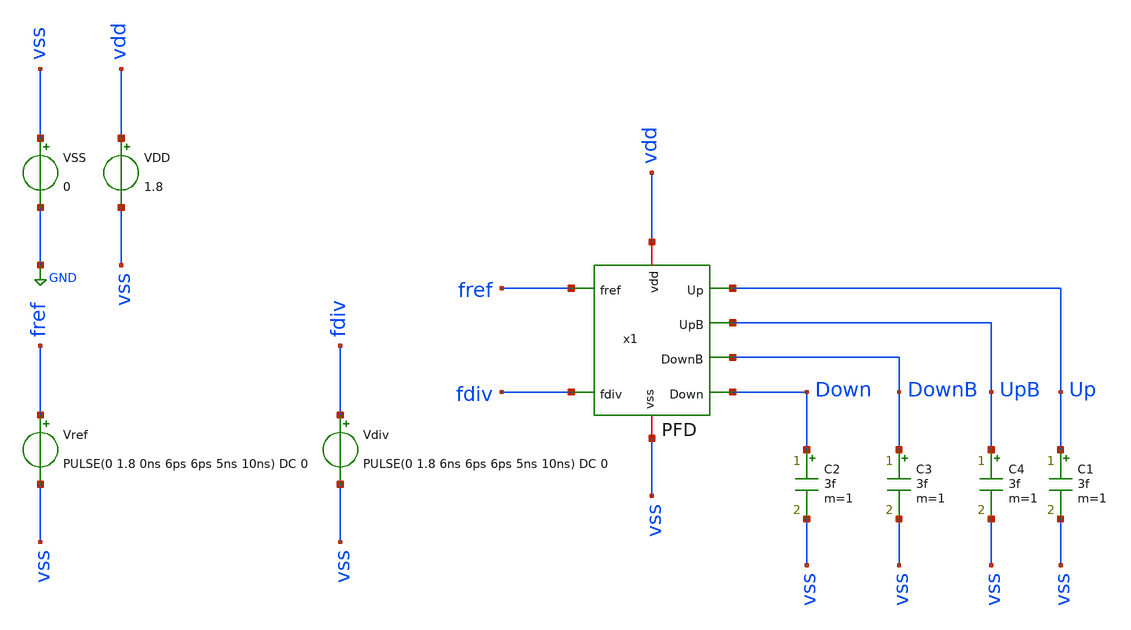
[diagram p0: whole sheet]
** sch_path: sch/PLL_caravel/tb_PFD.sch
**.subckt tb_PFD
VSS vss GND 0
VDD vdd vss 1.8
Vref fref vss PULSE(0 1.8 0ns 6ps 6ps 5ns 10ns) DC 0
Vdiv fdiv vss PULSE(0 1.8 6ns 6ps 6ps 5ns 10ns) DC 0
C1 Up vss 3f m=1
C2 Down vss 3f m=1
x1 vdd fref Up UpB DownB fdiv Down vss PFD
C3 DownB vss 3f m=1
C4 UpB vss 3f m=1
**** begin user architecture code



* Parameters
.options TEMPS = 27.0
.param wm1 = 0.64

* Models
.lib ~/skywater/skywater-pdk/libraries/sky130_fd_pr_ngspice/latest/models/corners/sky130.lib TT

* Data to save
.save all

* Simulation
.control
	tran 10n 300ns
        setplot tran1
        plot v(fref)+16 v(fdiv)+16 v(x1.out1)+14 v(x1.out2)+12 v(x1.out2)+10 v(x1.out4)+8 v(UpB)+6
+ v(DownB)+4 v(Up)+2 v(Down)
        set filetype = ascii
        write PFD_tran.raw
.endc

.end


**** end user architecture code
**.ends

* expanding   symbol:  PLL_caravel/PFD.sym # of pins=8
** sym_path: sch/PLL_caravel/PFD.sym
** sch_path: sch/PLL_caravel/PFD.sch
.subckt PFD vdd fref Up UpB DownB fdiv Down vss
*.ipin fref
*.iopin vdd
*.opin Down
*.ipin fdiv
*.iopin vss
*.opin Up
*.opin UpB
*.opin DownB
XM1 out1 fref vdd vdd sky130_fd_pr__pfet_01v8 L=0.15 W={wm1} nf=1 ad='int((nf+1)/2) * W/nf * 0.29' as='int((nf+2)/2) * W/nf * 0.29'
+ pd='2*int((nf+1)/2) * (W/nf + 0.29)' ps='2*int((nf+2)/2) * (W/nf + 0.29)' nrd='0.29 / W' nrs='0.29 / W'
+ sa=0 sb=0 sd=0 mult=1 m=1
XM2 out1 fref net1 vss sky130_fd_pr__nfet_01v8 L=0.15 W=1.8 nf=1 ad='int((nf+1)/2) * W/nf * 0.29' as='int((nf+2)/2) * W/nf * 0.29'
+ pd='2*int((nf+1)/2) * (W/nf + 0.29)' ps='2*int((nf+2)/2) * (W/nf + 0.29)' nrd='0.29 / W' nrs='0.29 / W'
+ sa=0 sb=0 sd=0 mult=1 m=1
XM3 net1 fdiv vss vss sky130_fd_pr__nfet_01v8 L=0.15 W=0.42 nf=1 ad='int((nf+1)/2) * W/nf * 0.29' as='int((nf+2)/2) * W/nf * 0.29'
+ pd='2*int((nf+1)/2) * (W/nf + 0.29)' ps='2*int((nf+2)/2) * (W/nf + 0.29)' nrd='0.29 / W' nrs='0.29 / W'
+ sa=0 sb=0 sd=0 mult=1 m=1
XM4 out2 fdiv vdd vdd sky130_fd_pr__pfet_01v8 L=0.15 W=0.64 nf=1 ad='int((nf+1)/2) * W/nf * 0.29' as='int((nf+2)/2) * W/nf * 0.29'
+ pd='2*int((nf+1)/2) * (W/nf + 0.29)' ps='2*int((nf+2)/2) * (W/nf + 0.29)' nrd='0.29 / W' nrs='0.29 / W'
+ sa=0 sb=0 sd=0 mult=1 m=1
XM5 out2 fdiv net2 vss sky130_fd_pr__nfet_01v8 L=0.15 W=1.8 nf=1 ad='int((nf+1)/2) * W/nf * 0.29' as='int((nf+2)/2) * W/nf * 0.29'
+ pd='2*int((nf+1)/2) * (W/nf + 0.29)' ps='2*int((nf+2)/2) * (W/nf + 0.29)' nrd='0.29 / W' nrs='0.29 / W'
+ sa=0 sb=0 sd=0 mult=1 m=1
XM6 net2 fref vss vss sky130_fd_pr__nfet_01v8 L=0.15 W=0.42 nf=1 ad='int((nf+1)/2) * W/nf * 0.29' as='int((nf+2)/2) * W/nf * 0.29'
+ pd='2*int((nf+1)/2) * (W/nf + 0.29)' ps='2*int((nf+2)/2) * (W/nf + 0.29)' nrd='0.29 / W' nrs='0.29 / W'
+ sa=0 sb=0 sd=0 mult=1 m=1
XM7 out3 fref fref vdd sky130_fd_pr__pfet_01v8 L=0.15 W=0.64 nf=1 ad='int((nf+1)/2) * W/nf * 0.29' as='int((nf+2)/2) * W/nf * 0.29'
+ pd='2*int((nf+1)/2) * (W/nf + 0.29)' ps='2*int((nf+2)/2) * (W/nf + 0.29)' nrd='0.29 / W' nrs='0.29 / W'
+ sa=0 sb=0 sd=0 mult=1 m=1
XM8 out3 fref out1 vss sky130_fd_pr__nfet_01v8 L=0.15 W=0.84 nf=1 ad='int((nf+1)/2) * W/nf * 0.29' as='int((nf+2)/2) * W/nf * 0.29'
+ pd='2*int((nf+1)/2) * (W/nf + 0.29)' ps='2*int((nf+2)/2) * (W/nf + 0.29)' nrd='0.29 / W' nrs='0.29 / W'
+ sa=0 sb=0 sd=0 mult=1 m=1
XM9 out4 fdiv fdiv vdd sky130_fd_pr__pfet_01v8 L=0.15 W=0.64 nf=1 ad='int((nf+1)/2) * W/nf * 0.29' as='int((nf+2)/2) * W/nf * 0.29'
+ pd='2*int((nf+1)/2) * (W/nf + 0.29)' ps='2*int((nf+2)/2) * (W/nf + 0.29)' nrd='0.29 / W' nrs='0.29 / W'
+ sa=0 sb=0 sd=0 mult=1 m=1
XM10 out4 fdiv out2 vss sky130_fd_pr__nfet_01v8 L=0.15 W=0.84 nf=1 ad='int((nf+1)/2) * W/nf * 0.29' as='int((nf+2)/2) * W/nf * 0.29'
+ pd='2*int((nf+1)/2) * (W/nf + 0.29)' ps='2*int((nf+2)/2) * (W/nf + 0.29)' nrd='0.29 / W' nrs='0.29 / W'
+ sa=0 sb=0 sd=0 mult=1 m=1
XM11 UpB out3 vdd vdd sky130_fd_pr__pfet_01v8 L=0.15 W=0.84 nf=1 ad='int((nf+1)/2) * W/nf * 0.29' as='int((nf+2)/2) * W/nf * 0.29'
+ pd='2*int((nf+1)/2) * (W/nf + 0.29)' ps='2*int((nf+2)/2) * (W/nf + 0.29)' nrd='0.29 / W' nrs='0.29 / W'
+ sa=0 sb=0 sd=0 mult=1 m=1
XM12 UpB out3 vss vss sky130_fd_pr__nfet_01v8 L=0.15 W=0.42 nf=1 ad='int((nf+1)/2) * W/nf * 0.29' as='int((nf+2)/2) * W/nf * 0.29'
+ pd='2*int((nf+1)/2) * (W/nf + 0.29)' ps='2*int((nf+2)/2) * (W/nf + 0.29)' nrd='0.29 / W' nrs='0.29 / W'
+ sa=0 sb=0 sd=0 mult=1 m=1
XM13 Up UpB vdd vdd sky130_fd_pr__pfet_01v8 L=0.15 W=0.96 nf=1 ad='int((nf+1)/2) * W/nf * 0.29' as='int((nf+2)/2) * W/nf * 0.29'
+ pd='2*int((nf+1)/2) * (W/nf + 0.29)' ps='2*int((nf+2)/2) * (W/nf + 0.29)' nrd='0.29 / W' nrs='0.29 / W'
+ sa=0 sb=0 sd=0 mult=1 m=1
XM14 Up UpB vss vss sky130_fd_pr__nfet_01v8 L=0.15 W=0.64 nf=1 ad='int((nf+1)/2) * W/nf * 0.29' as='int((nf+2)/2) * W/nf * 0.29'
+ pd='2*int((nf+1)/2) * (W/nf + 0.29)' ps='2*int((nf+2)/2) * (W/nf + 0.29)' nrd='0.29 / W' nrs='0.29 / W'
+ sa=0 sb=0 sd=0 mult=1 m=1
XM15 DownB out4 vdd vdd sky130_fd_pr__pfet_01v8 L=0.15 W=0.84 nf=1 ad='int((nf+1)/2) * W/nf * 0.29' as='int((nf+2)/2) * W/nf * 0.29'
+ pd='2*int((nf+1)/2) * (W/nf + 0.29)' ps='2*int((nf+2)/2) * (W/nf + 0.29)' nrd='0.29 / W' nrs='0.29 / W'
+ sa=0 sb=0 sd=0 mult=1 m=1
XM16 DownB out4 vss vss sky130_fd_pr__nfet_01v8 L=0.15 W=0.42 nf=1 ad='int((nf+1)/2) * W/nf * 0.29' as='int((nf+2)/2) * W/nf * 0.29'
+ pd='2*int((nf+1)/2) * (W/nf + 0.29)' ps='2*int((nf+2)/2) * (W/nf + 0.29)' nrd='0.29 / W' nrs='0.29 / W'
+ sa=0 sb=0 sd=0 mult=1 m=1
XM17 Down DownB vdd vdd sky130_fd_pr__pfet_01v8 L=0.15 W=0.96 nf=1 ad='int((nf+1)/2) * W/nf * 0.29' as='int((nf+2)/2) * W/nf * 0.29'
+ pd='2*int((nf+1)/2) * (W/nf + 0.29)' ps='2*int((nf+2)/2) * (W/nf + 0.29)' nrd='0.29 / W' nrs='0.29 / W'
+ sa=0 sb=0 sd=0 mult=1 m=1
XM18 Down DownB vss vss sky130_fd_pr__nfet_01v8 L=0.15 W=0.64 nf=1 ad='int((nf+1)/2) * W/nf * 0.29' as='int((nf+2)/2) * W/nf * 0.29'
+ pd='2*int((nf+1)/2) * (W/nf + 0.29)' ps='2*int((nf+2)/2) * (W/nf + 0.29)' nrd='0.29 / W' nrs='0.29 / W'
+ sa=0 sb=0 sd=0 mult=1 m=1
.ends

.GLOBAL GND
.end
